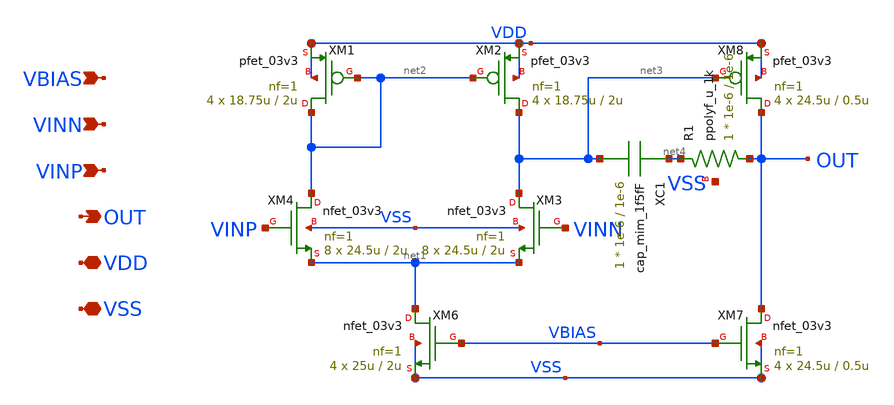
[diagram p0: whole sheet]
** sch_path: designs/libs/core_n-ota/nmos-ota/nmos-ota.sch
**.subckt nmos-ota VINN VINP OUT VDD VSS VBIAS
*.ipin VINN
*.ipin VINP
*.opin OUT
*.iopin VDD
*.iopin VSS
*.ipin VBIAS
XM1 net2 net2 VDD VDD pfet_03v3 L=2u W=18.75u nf=1 ad='int((nf+1)/2) * W/nf * 0.18u' as='int((nf+2)/2) * W/nf * 0.18u'
+ pd='2*int((nf+1)/2) * (W/nf + 0.18u)' ps='2*int((nf+2)/2) * (W/nf + 0.18u)' nrd='0.18u / W' nrs='0.18u / W'
+ sa=0 sb=0 sd=0 m=4
XM2 net3 net2 VDD VDD pfet_03v3 L=2u W=18.75u nf=1 ad='int((nf+1)/2) * W/nf * 0.18u' as='int((nf+2)/2) * W/nf * 0.18u'
+ pd='2*int((nf+1)/2) * (W/nf + 0.18u)' ps='2*int((nf+2)/2) * (W/nf + 0.18u)' nrd='0.18u / W' nrs='0.18u / W'
+ sa=0 sb=0 sd=0 m=4
XM3 net3 VINN net1 VSS nfet_03v3 L=2u W=24.5u nf=1 ad='int((nf+1)/2) * W/nf * 0.18u' as='int((nf+2)/2) * W/nf * 0.18u'
+ pd='2*int((nf+1)/2) * (W/nf + 0.18u)' ps='2*int((nf+2)/2) * (W/nf + 0.18u)' nrd='0.18u / W' nrs='0.18u / W'
+ sa=0 sb=0 sd=0 m=8
XM4 net2 VINP net1 VSS nfet_03v3 L=2u W=24.5u nf=1 ad='int((nf+1)/2) * W/nf * 0.18u' as='int((nf+2)/2) * W/nf * 0.18u'
+ pd='2*int((nf+1)/2) * (W/nf + 0.18u)' ps='2*int((nf+2)/2) * (W/nf + 0.18u)' nrd='0.18u / W' nrs='0.18u / W'
+ sa=0 sb=0 sd=0 m=8
XM6 net1 VBIAS VSS VSS nfet_03v3 L=2u W=25u nf=1 ad='int((nf+1)/2) * W/nf * 0.18u' as='int((nf+2)/2) * W/nf * 0.18u'
+ pd='2*int((nf+1)/2) * (W/nf + 0.18u)' ps='2*int((nf+2)/2) * (W/nf + 0.18u)' nrd='0.18u / W' nrs='0.18u / W'
+ sa=0 sb=0 sd=0 m=4
XM7 OUT VBIAS VSS VSS nfet_03v3 L=0.5u W=24.5u nf=1 ad='int((nf+1)/2) * W/nf * 0.18u' as='int((nf+2)/2) * W/nf * 0.18u'
+ pd='2*int((nf+1)/2) * (W/nf + 0.18u)' ps='2*int((nf+2)/2) * (W/nf + 0.18u)' nrd='0.18u / W' nrs='0.18u / W'
+ sa=0 sb=0 sd=0 m=4
XM8 OUT net3 VDD VDD pfet_03v3 L=0.5u W=24.5u nf=1 ad='int((nf+1)/2) * W/nf * 0.18u' as='int((nf+2)/2) * W/nf * 0.18u'
+ pd='2*int((nf+1)/2) * (W/nf + 0.18u)' ps='2*int((nf+2)/2) * (W/nf + 0.18u)' nrd='0.18u / W' nrs='0.18u / W'
+ sa=0 sb=0 sd=0 m=4
XC1 net4 net3 cap_mim_1f5fF c_width=1e-6 c_length=1e-6 m=1
XR1 OUT net4 VSS ppolyf_u_1k r_width=1e-6 r_length=1e-6 m=1
**.ends
.end
